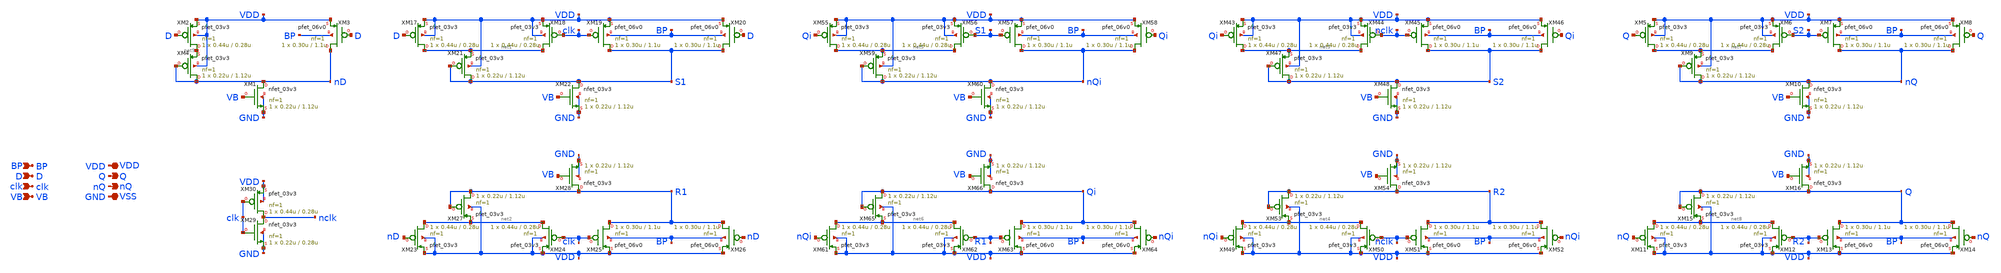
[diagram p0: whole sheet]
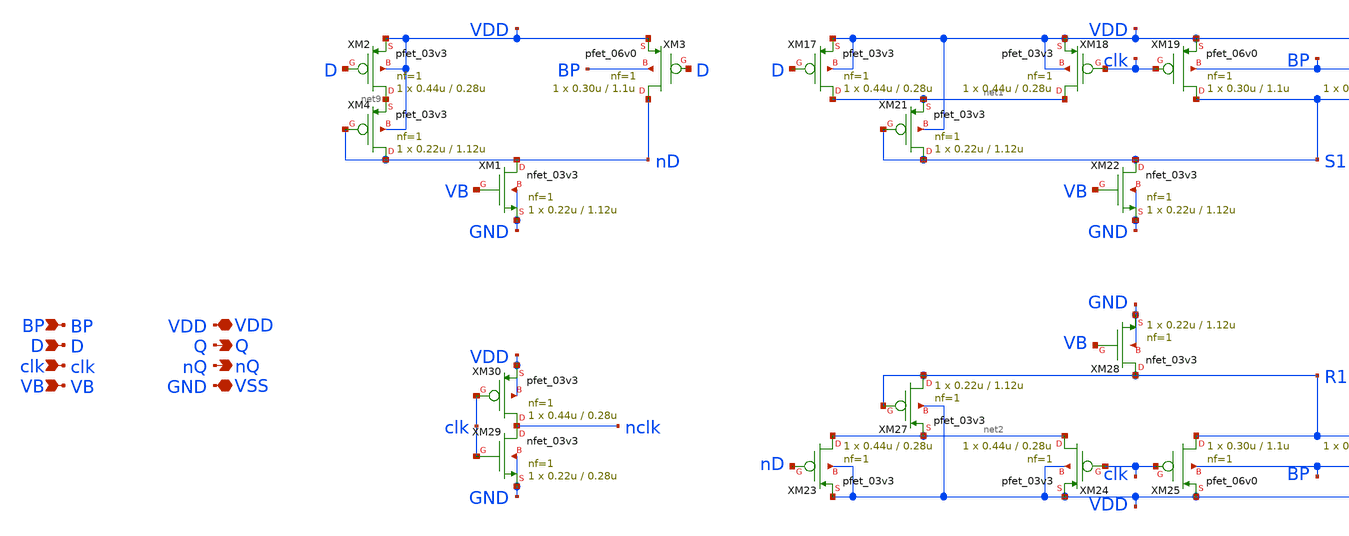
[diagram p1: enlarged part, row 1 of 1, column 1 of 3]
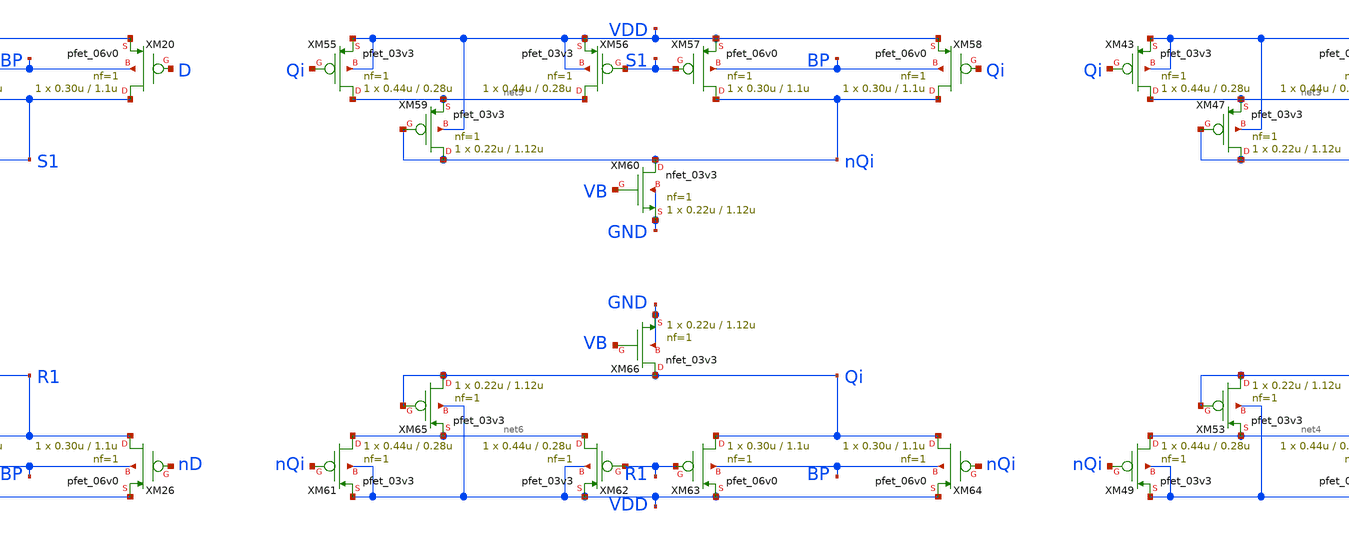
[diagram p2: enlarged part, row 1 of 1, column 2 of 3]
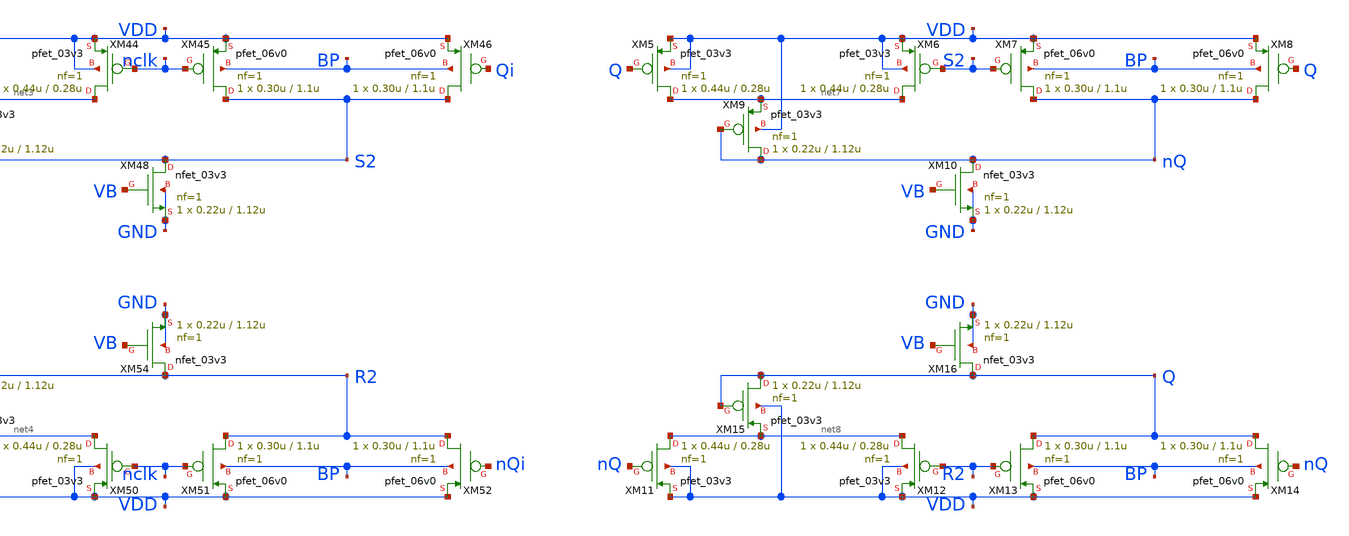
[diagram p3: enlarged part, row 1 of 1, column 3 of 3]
** sch_path: xschem_sn2/FF.sch
**.subckt FF D clk VDD Q VSS nQ VB BP
*.ipin D
*.ipin clk
*.iopin VDD
*.opin Q
*.iopin VSS
*.opin nQ
*.ipin VB
*.ipin BP
XM2 net9 D VDD VDD pfet_03v3 L=0.28u W=0.44u nf=1 ad='int((nf+1)/2) * W/nf * 0.18u' as='int((nf+2)/2) * W/nf * 0.18u'
+ pd='2*int((nf+1)/2) * (W/nf + 0.18u)' ps='2*int((nf+2)/2) * (W/nf + 0.18u)' nrd='0.18u / W' nrs='0.18u / W'
+ sa=0 sb=0 sd=0 m=1 par=1
XM3 nD D VDD BP pfet_06v0 L=1.1u W=0.30u nf=1 ad='int((nf+1)/2) * W/nf * 0.18u' as='int((nf+2)/2) * W/nf * 0.18u'
+ pd='2*int((nf+1)/2) * (W/nf + 0.18u)' ps='2*int((nf+2)/2) * (W/nf + 0.18u)' nrd='0.18u / W' nrs='0.18u / W'
+ sa=0 sb=0 sd=0 m=1
XM4 nD nD net9 VDD pfet_03v3 L=1.12u W=0.22u nf=1 ad='int((nf+1)/2) * W/nf * 0.18u' as='int((nf+2)/2) * W/nf * 0.18u'
+ pd='2*int((nf+1)/2) * (W/nf + 0.18u)' ps='2*int((nf+2)/2) * (W/nf + 0.18u)' nrd='0.18u / W' nrs='0.18u / W'
+ sa=0 sb=0 sd=0 m=1 par=1
XM17 net1 D VDD VDD pfet_03v3 L=0.28u W=0.44u nf=1 ad='int((nf+1)/2) * W/nf * 0.18u' as='int((nf+2)/2) * W/nf * 0.18u'
+ pd='2*int((nf+1)/2) * (W/nf + 0.18u)' ps='2*int((nf+2)/2) * (W/nf + 0.18u)' nrd='0.18u / W' nrs='0.18u / W'
+ sa=0 sb=0 sd=0 m=1 par=1
XM18 net1 clk VDD VDD pfet_03v3 L=0.28u W=0.44u nf=1 ad='int((nf+1)/2) * W/nf * 0.18u' as='int((nf+2)/2) * W/nf * 0.18u'
+ pd='2*int((nf+1)/2) * (W/nf + 0.18u)' ps='2*int((nf+2)/2) * (W/nf + 0.18u)' nrd='0.18u / W' nrs='0.18u / W'
+ sa=0 sb=0 sd=0 m=1 par=1
XM19 S1 clk VDD BP pfet_06v0 L=1.1u W=0.30u nf=1 ad='int((nf+1)/2) * W/nf * 0.18u' as='int((nf+2)/2) * W/nf * 0.18u'
+ pd='2*int((nf+1)/2) * (W/nf + 0.18u)' ps='2*int((nf+2)/2) * (W/nf + 0.18u)' nrd='0.18u / W' nrs='0.18u / W'
+ sa=0 sb=0 sd=0 m=1
XM20 S1 D VDD BP pfet_06v0 L=1.1u W=0.30u nf=1 ad='int((nf+1)/2) * W/nf * 0.18u' as='int((nf+2)/2) * W/nf * 0.18u'
+ pd='2*int((nf+1)/2) * (W/nf + 0.18u)' ps='2*int((nf+2)/2) * (W/nf + 0.18u)' nrd='0.18u / W' nrs='0.18u / W'
+ sa=0 sb=0 sd=0 m=1
XM21 S1 S1 net1 VDD pfet_03v3 L=1.12u W=0.22u nf=1 ad='int((nf+1)/2) * W/nf * 0.18u' as='int((nf+2)/2) * W/nf * 0.18u'
+ pd='2*int((nf+1)/2) * (W/nf + 0.18u)' ps='2*int((nf+2)/2) * (W/nf + 0.18u)' nrd='0.18u / W' nrs='0.18u / W'
+ sa=0 sb=0 sd=0 m=1 par=1
XM22 S1 VB GND GND nfet_03v3 L=1.12u W=0.22u nf=1 ad='int((nf+1)/2) * W/nf * 0.18u' as='int((nf+2)/2) * W/nf * 0.18u'
+ pd='2*int((nf+1)/2) * (W/nf + 0.18u)' ps='2*int((nf+2)/2) * (W/nf + 0.18u)' nrd='0.18u / W' nrs='0.18u / W'
+ sa=0 sb=0 sd=0 m=1 par=1
XM23 net2 nD VDD VDD pfet_03v3 L=0.28u W=0.44u nf=1 ad='int((nf+1)/2) * W/nf * 0.18u' as='int((nf+2)/2) * W/nf * 0.18u'
+ pd='2*int((nf+1)/2) * (W/nf + 0.18u)' ps='2*int((nf+2)/2) * (W/nf + 0.18u)' nrd='0.18u / W' nrs='0.18u / W'
+ sa=0 sb=0 sd=0 m=1 par=1
XM24 net2 clk VDD VDD pfet_03v3 L=0.28u W=0.44u nf=1 ad='int((nf+1)/2) * W/nf * 0.18u' as='int((nf+2)/2) * W/nf * 0.18u'
+ pd='2*int((nf+1)/2) * (W/nf + 0.18u)' ps='2*int((nf+2)/2) * (W/nf + 0.18u)' nrd='0.18u / W' nrs='0.18u / W'
+ sa=0 sb=0 sd=0 m=1 par=1
XM25 R1 clk VDD BP pfet_06v0 L=1.1u W=0.30u nf=1 ad='int((nf+1)/2) * W/nf * 0.18u' as='int((nf+2)/2) * W/nf * 0.18u'
+ pd='2*int((nf+1)/2) * (W/nf + 0.18u)' ps='2*int((nf+2)/2) * (W/nf + 0.18u)' nrd='0.18u / W' nrs='0.18u / W'
+ sa=0 sb=0 sd=0 m=1
XM26 R1 nD VDD BP pfet_06v0 L=1.1u W=0.30u nf=1 ad='int((nf+1)/2) * W/nf * 0.18u' as='int((nf+2)/2) * W/nf * 0.18u'
+ pd='2*int((nf+1)/2) * (W/nf + 0.18u)' ps='2*int((nf+2)/2) * (W/nf + 0.18u)' nrd='0.18u / W' nrs='0.18u / W'
+ sa=0 sb=0 sd=0 m=1
XM27 R1 R1 net2 VDD pfet_03v3 L=1.12u W=0.22u nf=1 ad='int((nf+1)/2) * W/nf * 0.18u' as='int((nf+2)/2) * W/nf * 0.18u'
+ pd='2*int((nf+1)/2) * (W/nf + 0.18u)' ps='2*int((nf+2)/2) * (W/nf + 0.18u)' nrd='0.18u / W' nrs='0.18u / W'
+ sa=0 sb=0 sd=0 m=1 par=1
XM28 R1 VB GND GND nfet_03v3 L=1.12u W=0.22u nf=1 ad='int((nf+1)/2) * W/nf * 0.18u' as='int((nf+2)/2) * W/nf * 0.18u'
+ pd='2*int((nf+1)/2) * (W/nf + 0.18u)' ps='2*int((nf+2)/2) * (W/nf + 0.18u)' nrd='0.18u / W' nrs='0.18u / W'
+ sa=0 sb=0 sd=0 m=1 par=1
XM29 nclk clk GND GND nfet_03v3 L=0.28u W=0.22u nf=1 ad='int((nf+1)/2) * W/nf * 0.18u' as='int((nf+2)/2) * W/nf * 0.18u'
+ pd='2*int((nf+1)/2) * (W/nf + 0.18u)' ps='2*int((nf+2)/2) * (W/nf + 0.18u)' nrd='0.18u / W' nrs='0.18u / W'
+ sa=0 sb=0 sd=0 m=1 par=1
XM30 nclk clk VDD VDD pfet_03v3 L=0.28u W=0.44u nf=1 ad='int((nf+1)/2) * W/nf * 0.18u' as='int((nf+2)/2) * W/nf * 0.18u'
+ pd='2*int((nf+1)/2) * (W/nf + 0.18u)' ps='2*int((nf+2)/2) * (W/nf + 0.18u)' nrd='0.18u / W' nrs='0.18u / W'
+ sa=0 sb=0 sd=0 m=1 par=1
XM1 nD VB GND GND nfet_03v3 L=1.12u W=0.22u nf=1 ad='int((nf+1)/2) * W/nf * 0.18u' as='int((nf+2)/2) * W/nf * 0.18u'
+ pd='2*int((nf+1)/2) * (W/nf + 0.18u)' ps='2*int((nf+2)/2) * (W/nf + 0.18u)' nrd='0.18u / W' nrs='0.18u / W'
+ sa=0 sb=0 sd=0 m=1 par=1
XM43 net3 Qi VDD VDD pfet_03v3 L=0.28u W=0.44u nf=1 ad='int((nf+1)/2) * W/nf * 0.18u' as='int((nf+2)/2) * W/nf * 0.18u'
+ pd='2*int((nf+1)/2) * (W/nf + 0.18u)' ps='2*int((nf+2)/2) * (W/nf + 0.18u)' nrd='0.18u / W' nrs='0.18u / W'
+ sa=0 sb=0 sd=0 m=1 par=1
XM44 net3 nclk VDD VDD pfet_03v3 L=0.28u W=0.44u nf=1 ad='int((nf+1)/2) * W/nf * 0.18u' as='int((nf+2)/2) * W/nf * 0.18u'
+ pd='2*int((nf+1)/2) * (W/nf + 0.18u)' ps='2*int((nf+2)/2) * (W/nf + 0.18u)' nrd='0.18u / W' nrs='0.18u / W'
+ sa=0 sb=0 sd=0 m=1 par=1
XM45 S2 nclk VDD BP pfet_06v0 L=1.1u W=0.30u nf=1 ad='int((nf+1)/2) * W/nf * 0.18u' as='int((nf+2)/2) * W/nf * 0.18u'
+ pd='2*int((nf+1)/2) * (W/nf + 0.18u)' ps='2*int((nf+2)/2) * (W/nf + 0.18u)' nrd='0.18u / W' nrs='0.18u / W'
+ sa=0 sb=0 sd=0 m=1
XM46 S2 Qi VDD BP pfet_06v0 L=1.1u W=0.30u nf=1 ad='int((nf+1)/2) * W/nf * 0.18u' as='int((nf+2)/2) * W/nf * 0.18u'
+ pd='2*int((nf+1)/2) * (W/nf + 0.18u)' ps='2*int((nf+2)/2) * (W/nf + 0.18u)' nrd='0.18u / W' nrs='0.18u / W'
+ sa=0 sb=0 sd=0 m=1
XM47 S2 S2 net3 VDD pfet_03v3 L=1.12u W=0.22u nf=1 ad='int((nf+1)/2) * W/nf * 0.18u' as='int((nf+2)/2) * W/nf * 0.18u'
+ pd='2*int((nf+1)/2) * (W/nf + 0.18u)' ps='2*int((nf+2)/2) * (W/nf + 0.18u)' nrd='0.18u / W' nrs='0.18u / W'
+ sa=0 sb=0 sd=0 m=1 par=1
XM48 S2 VB GND GND nfet_03v3 L=1.12u W=0.22u nf=1 ad='int((nf+1)/2) * W/nf * 0.18u' as='int((nf+2)/2) * W/nf * 0.18u'
+ pd='2*int((nf+1)/2) * (W/nf + 0.18u)' ps='2*int((nf+2)/2) * (W/nf + 0.18u)' nrd='0.18u / W' nrs='0.18u / W'
+ sa=0 sb=0 sd=0 m=1 par=1
XM49 net4 nQi VDD VDD pfet_03v3 L=0.28u W=0.44u nf=1 ad='int((nf+1)/2) * W/nf * 0.18u' as='int((nf+2)/2) * W/nf * 0.18u'
+ pd='2*int((nf+1)/2) * (W/nf + 0.18u)' ps='2*int((nf+2)/2) * (W/nf + 0.18u)' nrd='0.18u / W' nrs='0.18u / W'
+ sa=0 sb=0 sd=0 m=1 par=1
XM50 net4 nclk VDD VDD pfet_03v3 L=0.28u W=0.44u nf=1 ad='int((nf+1)/2) * W/nf * 0.18u' as='int((nf+2)/2) * W/nf * 0.18u'
+ pd='2*int((nf+1)/2) * (W/nf + 0.18u)' ps='2*int((nf+2)/2) * (W/nf + 0.18u)' nrd='0.18u / W' nrs='0.18u / W'
+ sa=0 sb=0 sd=0 m=1 par=1
XM51 R2 nclk VDD BP pfet_06v0 L=1.1u W=0.30u nf=1 ad='int((nf+1)/2) * W/nf * 0.18u' as='int((nf+2)/2) * W/nf * 0.18u'
+ pd='2*int((nf+1)/2) * (W/nf + 0.18u)' ps='2*int((nf+2)/2) * (W/nf + 0.18u)' nrd='0.18u / W' nrs='0.18u / W'
+ sa=0 sb=0 sd=0 m=1
XM52 R2 nQi VDD BP pfet_06v0 L=1.1u W=0.30u nf=1 ad='int((nf+1)/2) * W/nf * 0.18u' as='int((nf+2)/2) * W/nf * 0.18u'
+ pd='2*int((nf+1)/2) * (W/nf + 0.18u)' ps='2*int((nf+2)/2) * (W/nf + 0.18u)' nrd='0.18u / W' nrs='0.18u / W'
+ sa=0 sb=0 sd=0 m=1
XM53 R2 R2 net4 VDD pfet_03v3 L=1.12u W=0.22u nf=1 ad='int((nf+1)/2) * W/nf * 0.18u' as='int((nf+2)/2) * W/nf * 0.18u'
+ pd='2*int((nf+1)/2) * (W/nf + 0.18u)' ps='2*int((nf+2)/2) * (W/nf + 0.18u)' nrd='0.18u / W' nrs='0.18u / W'
+ sa=0 sb=0 sd=0 m=1 par=1
XM54 R2 VB GND GND nfet_03v3 L=1.12u W=0.22u nf=1 ad='int((nf+1)/2) * W/nf * 0.18u' as='int((nf+2)/2) * W/nf * 0.18u'
+ pd='2*int((nf+1)/2) * (W/nf + 0.18u)' ps='2*int((nf+2)/2) * (W/nf + 0.18u)' nrd='0.18u / W' nrs='0.18u / W'
+ sa=0 sb=0 sd=0 m=1 par=1
XM55 net5 Qi VDD VDD pfet_03v3 L=0.28u W=0.44u nf=1 ad='int((nf+1)/2) * W/nf * 0.18u' as='int((nf+2)/2) * W/nf * 0.18u'
+ pd='2*int((nf+1)/2) * (W/nf + 0.18u)' ps='2*int((nf+2)/2) * (W/nf + 0.18u)' nrd='0.18u / W' nrs='0.18u / W'
+ sa=0 sb=0 sd=0 m=1 par=1
XM56 net5 S1 VDD VDD pfet_03v3 L=0.28u W=0.44u nf=1 ad='int((nf+1)/2) * W/nf * 0.18u' as='int((nf+2)/2) * W/nf * 0.18u'
+ pd='2*int((nf+1)/2) * (W/nf + 0.18u)' ps='2*int((nf+2)/2) * (W/nf + 0.18u)' nrd='0.18u / W' nrs='0.18u / W'
+ sa=0 sb=0 sd=0 m=1 par=1
XM57 nQi S1 VDD BP pfet_06v0 L=1.1u W=0.30u nf=1 ad='int((nf+1)/2) * W/nf * 0.18u' as='int((nf+2)/2) * W/nf * 0.18u'
+ pd='2*int((nf+1)/2) * (W/nf + 0.18u)' ps='2*int((nf+2)/2) * (W/nf + 0.18u)' nrd='0.18u / W' nrs='0.18u / W'
+ sa=0 sb=0 sd=0 m=1
XM58 nQi Qi VDD BP pfet_06v0 L=1.1u W=0.30u nf=1 ad='int((nf+1)/2) * W/nf * 0.18u' as='int((nf+2)/2) * W/nf * 0.18u'
+ pd='2*int((nf+1)/2) * (W/nf + 0.18u)' ps='2*int((nf+2)/2) * (W/nf + 0.18u)' nrd='0.18u / W' nrs='0.18u / W'
+ sa=0 sb=0 sd=0 m=1
XM59 nQi nQi net5 VDD pfet_03v3 L=1.12u W=0.22u nf=1 ad='int((nf+1)/2) * W/nf * 0.18u' as='int((nf+2)/2) * W/nf * 0.18u'
+ pd='2*int((nf+1)/2) * (W/nf + 0.18u)' ps='2*int((nf+2)/2) * (W/nf + 0.18u)' nrd='0.18u / W' nrs='0.18u / W'
+ sa=0 sb=0 sd=0 m=1 par=1
XM60 nQi VB GND GND nfet_03v3 L=1.12u W=0.22u nf=1 ad='int((nf+1)/2) * W/nf * 0.18u' as='int((nf+2)/2) * W/nf * 0.18u'
+ pd='2*int((nf+1)/2) * (W/nf + 0.18u)' ps='2*int((nf+2)/2) * (W/nf + 0.18u)' nrd='0.18u / W' nrs='0.18u / W'
+ sa=0 sb=0 sd=0 m=1 par=1
XM61 net6 nQi VDD VDD pfet_03v3 L=0.28u W=0.44u nf=1 ad='int((nf+1)/2) * W/nf * 0.18u' as='int((nf+2)/2) * W/nf * 0.18u'
+ pd='2*int((nf+1)/2) * (W/nf + 0.18u)' ps='2*int((nf+2)/2) * (W/nf + 0.18u)' nrd='0.18u / W' nrs='0.18u / W'
+ sa=0 sb=0 sd=0 m=1 par=1
XM62 net6 R1 VDD VDD pfet_03v3 L=0.28u W=0.44u nf=1 ad='int((nf+1)/2) * W/nf * 0.18u' as='int((nf+2)/2) * W/nf * 0.18u'
+ pd='2*int((nf+1)/2) * (W/nf + 0.18u)' ps='2*int((nf+2)/2) * (W/nf + 0.18u)' nrd='0.18u / W' nrs='0.18u / W'
+ sa=0 sb=0 sd=0 m=1 par=1
XM63 Qi R1 VDD BP pfet_06v0 L=1.1u W=0.30u nf=1 ad='int((nf+1)/2) * W/nf * 0.18u' as='int((nf+2)/2) * W/nf * 0.18u'
+ pd='2*int((nf+1)/2) * (W/nf + 0.18u)' ps='2*int((nf+2)/2) * (W/nf + 0.18u)' nrd='0.18u / W' nrs='0.18u / W'
+ sa=0 sb=0 sd=0 m=1
XM64 Qi nQi VDD BP pfet_06v0 L=1.1u W=0.30u nf=1 ad='int((nf+1)/2) * W/nf * 0.18u' as='int((nf+2)/2) * W/nf * 0.18u'
+ pd='2*int((nf+1)/2) * (W/nf + 0.18u)' ps='2*int((nf+2)/2) * (W/nf + 0.18u)' nrd='0.18u / W' nrs='0.18u / W'
+ sa=0 sb=0 sd=0 m=1
XM65 Qi Qi net6 VDD pfet_03v3 L=1.12u W=0.22u nf=1 ad='int((nf+1)/2) * W/nf * 0.18u' as='int((nf+2)/2) * W/nf * 0.18u'
+ pd='2*int((nf+1)/2) * (W/nf + 0.18u)' ps='2*int((nf+2)/2) * (W/nf + 0.18u)' nrd='0.18u / W' nrs='0.18u / W'
+ sa=0 sb=0 sd=0 m=1 par=1
XM66 Qi VB GND GND nfet_03v3 L=1.12u W=0.22u nf=1 ad='int((nf+1)/2) * W/nf * 0.18u' as='int((nf+2)/2) * W/nf * 0.18u'
+ pd='2*int((nf+1)/2) * (W/nf + 0.18u)' ps='2*int((nf+2)/2) * (W/nf + 0.18u)' nrd='0.18u / W' nrs='0.18u / W'
+ sa=0 sb=0 sd=0 m=1 par=1
XM5 net7 Q VDD VDD pfet_03v3 L=0.28u W=0.44u nf=1 ad='int((nf+1)/2) * W/nf * 0.18u' as='int((nf+2)/2) * W/nf * 0.18u'
+ pd='2*int((nf+1)/2) * (W/nf + 0.18u)' ps='2*int((nf+2)/2) * (W/nf + 0.18u)' nrd='0.18u / W' nrs='0.18u / W'
+ sa=0 sb=0 sd=0 m=1 par=1
XM6 net7 S2 VDD VDD pfet_03v3 L=0.28u W=0.44u nf=1 ad='int((nf+1)/2) * W/nf * 0.18u' as='int((nf+2)/2) * W/nf * 0.18u'
+ pd='2*int((nf+1)/2) * (W/nf + 0.18u)' ps='2*int((nf+2)/2) * (W/nf + 0.18u)' nrd='0.18u / W' nrs='0.18u / W'
+ sa=0 sb=0 sd=0 m=1 par=1
XM7 nQ S2 VDD BP pfet_06v0 L=1.1u W=0.30u nf=1 ad='int((nf+1)/2) * W/nf * 0.18u' as='int((nf+2)/2) * W/nf * 0.18u'
+ pd='2*int((nf+1)/2) * (W/nf + 0.18u)' ps='2*int((nf+2)/2) * (W/nf + 0.18u)' nrd='0.18u / W' nrs='0.18u / W'
+ sa=0 sb=0 sd=0 m=1
XM8 nQ Q VDD BP pfet_06v0 L=1.1u W=0.30u nf=1 ad='int((nf+1)/2) * W/nf * 0.18u' as='int((nf+2)/2) * W/nf * 0.18u'
+ pd='2*int((nf+1)/2) * (W/nf + 0.18u)' ps='2*int((nf+2)/2) * (W/nf + 0.18u)' nrd='0.18u / W' nrs='0.18u / W'
+ sa=0 sb=0 sd=0 m=1
XM9 nQ nQ net7 VDD pfet_03v3 L=1.12u W=0.22u nf=1 ad='int((nf+1)/2) * W/nf * 0.18u' as='int((nf+2)/2) * W/nf * 0.18u'
+ pd='2*int((nf+1)/2) * (W/nf + 0.18u)' ps='2*int((nf+2)/2) * (W/nf + 0.18u)' nrd='0.18u / W' nrs='0.18u / W'
+ sa=0 sb=0 sd=0 m=1 par=1
XM10 nQ VB GND GND nfet_03v3 L=1.12u W=0.22u nf=1 ad='int((nf+1)/2) * W/nf * 0.18u' as='int((nf+2)/2) * W/nf * 0.18u'
+ pd='2*int((nf+1)/2) * (W/nf + 0.18u)' ps='2*int((nf+2)/2) * (W/nf + 0.18u)' nrd='0.18u / W' nrs='0.18u / W'
+ sa=0 sb=0 sd=0 m=1 par=1
XM11 net8 nQ VDD VDD pfet_03v3 L=0.28u W=0.44u nf=1 ad='int((nf+1)/2) * W/nf * 0.18u' as='int((nf+2)/2) * W/nf * 0.18u'
+ pd='2*int((nf+1)/2) * (W/nf + 0.18u)' ps='2*int((nf+2)/2) * (W/nf + 0.18u)' nrd='0.18u / W' nrs='0.18u / W'
+ sa=0 sb=0 sd=0 m=1 par=1
XM12 net8 R2 VDD VDD pfet_03v3 L=0.28u W=0.44u nf=1 ad='int((nf+1)/2) * W/nf * 0.18u' as='int((nf+2)/2) * W/nf * 0.18u'
+ pd='2*int((nf+1)/2) * (W/nf + 0.18u)' ps='2*int((nf+2)/2) * (W/nf + 0.18u)' nrd='0.18u / W' nrs='0.18u / W'
+ sa=0 sb=0 sd=0 m=1 par=1
XM13 Q R2 VDD BP pfet_06v0 L=1.1u W=0.30u nf=1 ad='int((nf+1)/2) * W/nf * 0.18u' as='int((nf+2)/2) * W/nf * 0.18u'
+ pd='2*int((nf+1)/2) * (W/nf + 0.18u)' ps='2*int((nf+2)/2) * (W/nf + 0.18u)' nrd='0.18u / W' nrs='0.18u / W'
+ sa=0 sb=0 sd=0 m=1
XM14 Q nQ VDD BP pfet_06v0 L=1.1u W=0.30u nf=1 ad='int((nf+1)/2) * W/nf * 0.18u' as='int((nf+2)/2) * W/nf * 0.18u'
+ pd='2*int((nf+1)/2) * (W/nf + 0.18u)' ps='2*int((nf+2)/2) * (W/nf + 0.18u)' nrd='0.18u / W' nrs='0.18u / W'
+ sa=0 sb=0 sd=0 m=1
XM15 Q Q net8 VDD pfet_03v3 L=1.12u W=0.22u nf=1 ad='int((nf+1)/2) * W/nf * 0.18u' as='int((nf+2)/2) * W/nf * 0.18u'
+ pd='2*int((nf+1)/2) * (W/nf + 0.18u)' ps='2*int((nf+2)/2) * (W/nf + 0.18u)' nrd='0.18u / W' nrs='0.18u / W'
+ sa=0 sb=0 sd=0 m=1 par=1
XM16 Q VB GND GND nfet_03v3 L=1.12u W=0.22u nf=1 ad='int((nf+1)/2) * W/nf * 0.18u' as='int((nf+2)/2) * W/nf * 0.18u'
+ pd='2*int((nf+1)/2) * (W/nf + 0.18u)' ps='2*int((nf+2)/2) * (W/nf + 0.18u)' nrd='0.18u / W' nrs='0.18u / W'
+ sa=0 sb=0 sd=0 m=1 par=1
**.ends
.end
